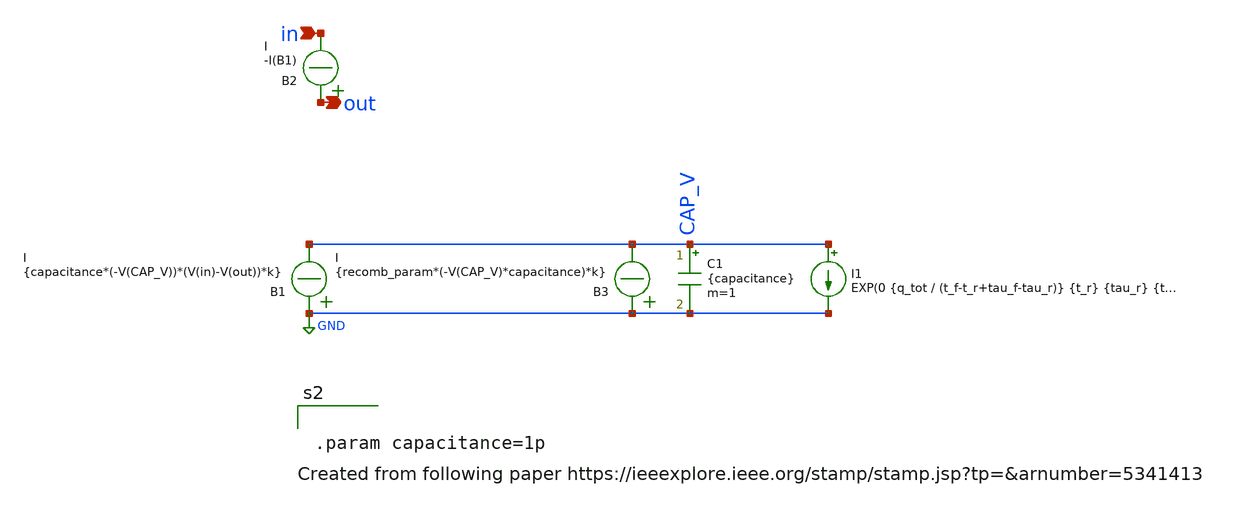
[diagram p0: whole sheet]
** sch_path: lib/Organize_into_Examples_or_pdk_examples/xschem_rad_library/adaptive_double_exp.sch
**.subckt adaptive_double_exp in out
*.ipin in
*.opin out
B2 out in I = -I(B1)
B1 GND CAP_V I = {capacitance*(-V(CAP_V))*(V(in)-V(out))*k}
B3 GND CAP_V I = {recomb_param*(-V(CAP_V)*capacitance)*k}
C1 CAP_V GND {capacitance} m=1
I1 CAP_V GND EXP(0 {q_tot / (t_f-t_r+tau_f-tau_r)} {t_r} {tau_r} {t_f} {tau_f})
**** begin user architecture code


.param capacitance=1p


**** end user architecture code
**.ends
.GLOBAL GND
.end
